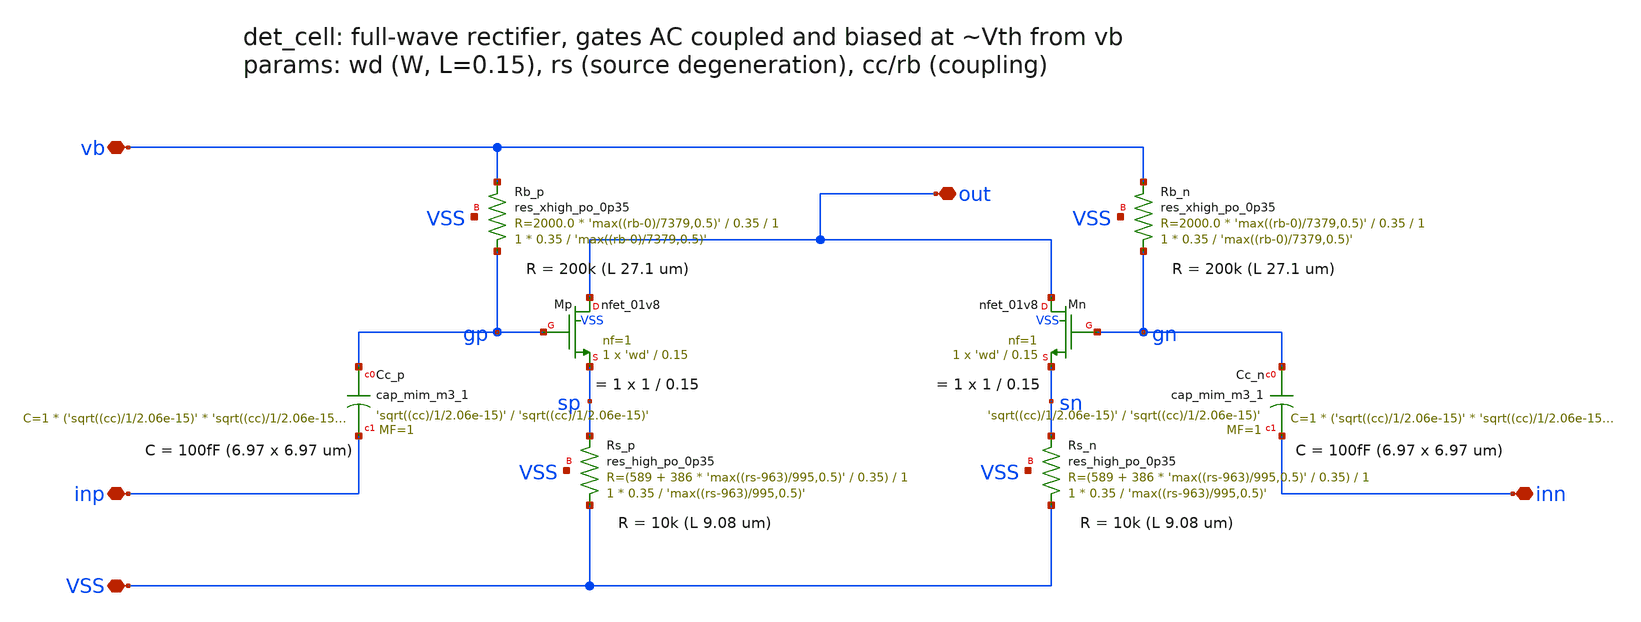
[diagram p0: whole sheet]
** sch_path: xschem/det_cell.sch
**.subckt det_cell VSS vb inp inn out
*.iopin VSS
*.iopin vb
*.iopin inp
*.iopin inn
*.iopin out
XCc_p gp inp sky130_fd_pr__cap_mim_m3_1 W='sqrt((cc)/1/2.06e-15)' L='sqrt((cc)/1/2.06e-15)' MF=1 m=1
XRb_p gp vb VSS sky130_fd_pr__res_xhigh_po_0p35 L='max((rb-0)/7379,0.5)' mult=1 m=1
XMp out gp sp VSS sky130_fd_pr__nfet_01v8 L=0.15 W='wd' nf=1 ad='int((nf+1)/2) * W/nf * 0.29' as='int((nf+2)/2) * W/nf * 0.29'
+ pd='2*int((nf+1)/2) * (W/nf + 0.29)' ps='2*int((nf+2)/2) * (W/nf + 0.29)' nrd='0.29 / W' nrs='0.29 / W'
+ sa=0 sb=0 sd=0 mult=1 m=1
XRs_p VSS sp VSS sky130_fd_pr__res_high_po_0p35 L='max((rs-963)/995,0.5)' mult=1 m=1
XCc_n gn inn sky130_fd_pr__cap_mim_m3_1 W='sqrt((cc)/1/2.06e-15)' L='sqrt((cc)/1/2.06e-15)' MF=1 m=1
XRb_n gn vb VSS sky130_fd_pr__res_xhigh_po_0p35 L='max((rb-0)/7379,0.5)' mult=1 m=1
XMn out gn sn VSS sky130_fd_pr__nfet_01v8 L=0.15 W='wd' nf=1 ad='int((nf+1)/2) * W/nf * 0.29' as='int((nf+2)/2) * W/nf * 0.29'
+ pd='2*int((nf+1)/2) * (W/nf + 0.29)' ps='2*int((nf+2)/2) * (W/nf + 0.29)' nrd='0.29 / W' nrs='0.29 / W'
+ sa=0 sb=0 sd=0 mult=1 m=1
XRs_n VSS sn VSS sky130_fd_pr__res_high_po_0p35 L='max((rs-963)/995,0.5)' mult=1 m=1
**.ends
.end
